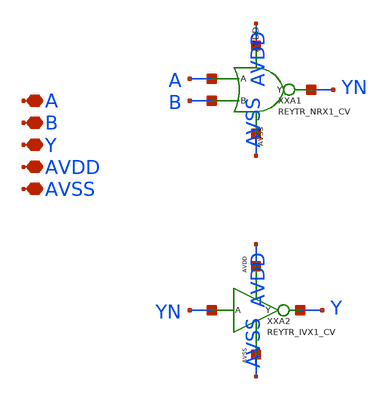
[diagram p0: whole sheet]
** sch_path: design/REY_TR_SKY130A/REYTR_ORX1_CV.sch
**.subckt REYTR_ORX1_CV A B Y AVDD AVSS
*.iopin A
*.iopin B
*.iopin Y
*.iopin AVDD
*.iopin AVSS
XXA1 A B YN AVDD AVSS REYTR_NRX1_CV
XXA2 YN Y AVDD AVSS REYTR_IVX1_CV
**.ends
.end
